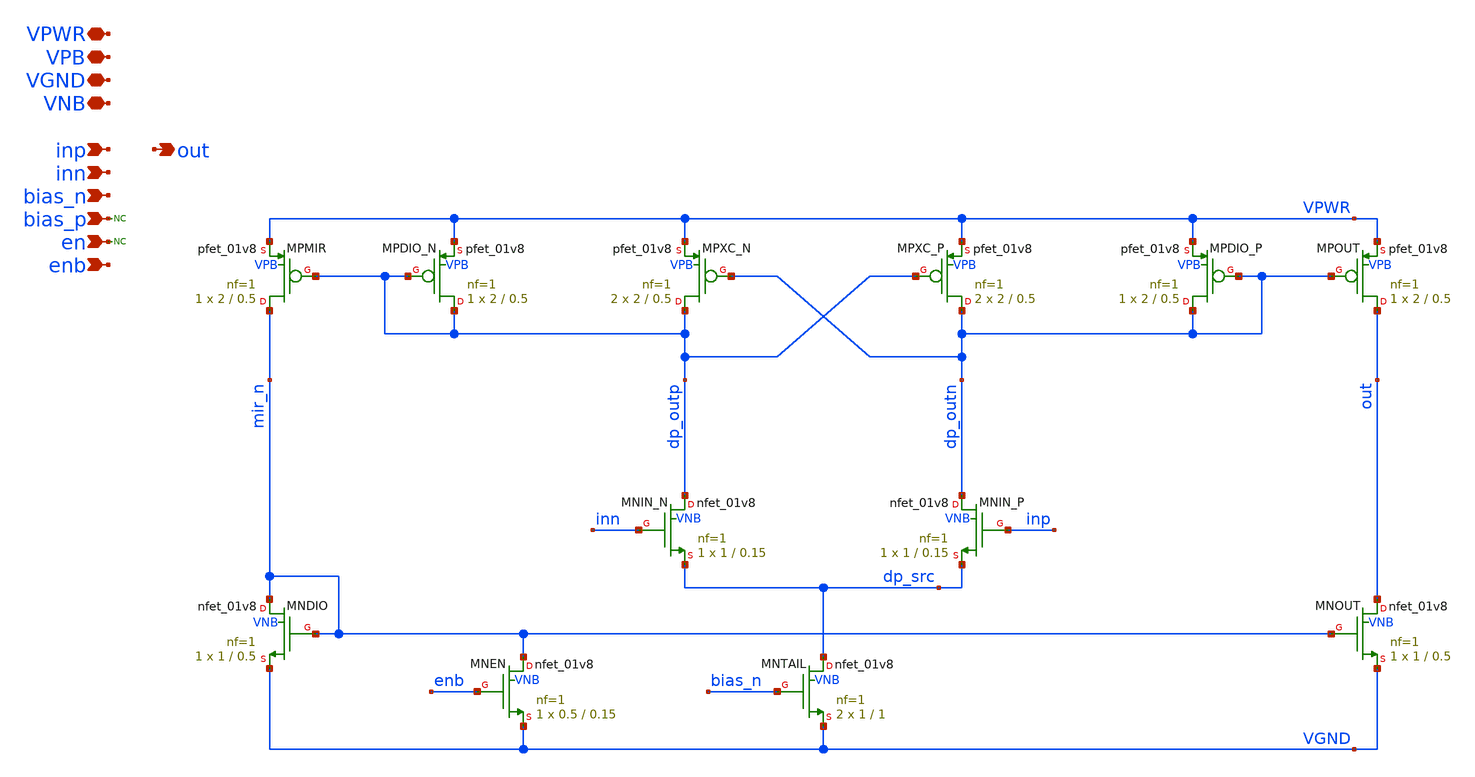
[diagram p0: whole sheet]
** sch_path: xschem/tiny_adc/tiny_adc_comp.sch
**.subckt tiny_adc_comp VPWR VPB VGND VNB inp out inn bias_n bias_p en enb
*.iopin VPWR
*.iopin VPB
*.iopin VGND
*.iopin VNB
*.ipin inp
*.opin out
*.ipin inn
*.ipin bias_n
*.ipin bias_p
*.ipin en
*.ipin enb
XMNIN_N dp_outp inn dp_src VNB sky130_fd_pr__nfet_01v8 L=0.15 W=1 nf=1 ad='int((nf+1)/2) * W/nf * 0.29'
+ as='int((nf+2)/2) * W/nf * 0.29' pd='2*int((nf+1)/2) * (W/nf + 0.29)' ps='2*int((nf+2)/2) * (W/nf + 0.29)'
+ nrd='0.29 / W' nrs='0.29 / W' sa=0 sb=0 sd=0 mult=1 m=1
XMNIN_P dp_outn inp dp_src VNB sky130_fd_pr__nfet_01v8 L=0.15 W=1 nf=1 ad='int((nf+1)/2) * W/nf * 0.29'
+ as='int((nf+2)/2) * W/nf * 0.29' pd='2*int((nf+1)/2) * (W/nf + 0.29)' ps='2*int((nf+2)/2) * (W/nf + 0.29)'
+ nrd='0.29 / W' nrs='0.29 / W' sa=0 sb=0 sd=0 mult=1 m=1
XMNTAIL dp_src bias_n VGND VNB sky130_fd_pr__nfet_01v8 L=1 W=1 nf=1 ad='int((nf+1)/2) * W/nf * 0.29'
+ as='int((nf+2)/2) * W/nf * 0.29' pd='2*int((nf+1)/2) * (W/nf + 0.29)' ps='2*int((nf+2)/2) * (W/nf + 0.29)'
+ nrd='0.29 / W' nrs='0.29 / W' sa=0 sb=0 sd=0 mult=2 m=2
XMPXC_P dp_outn dp_outp VPWR VPB sky130_fd_pr__pfet_01v8 L=0.5 W=2 nf=1 ad='int((nf+1)/2) * W/nf * 0.29'
+ as='int((nf+2)/2) * W/nf * 0.29' pd='2*int((nf+1)/2) * (W/nf + 0.29)' ps='2*int((nf+2)/2) * (W/nf + 0.29)'
+ nrd='0.29 / W' nrs='0.29 / W' sa=0 sb=0 sd=0 mult=2 m=2
XMPXC_N dp_outp dp_outn VPWR VPB sky130_fd_pr__pfet_01v8 L=0.5 W=2 nf=1 ad='int((nf+1)/2) * W/nf * 0.29'
+ as='int((nf+2)/2) * W/nf * 0.29' pd='2*int((nf+1)/2) * (W/nf + 0.29)' ps='2*int((nf+2)/2) * (W/nf + 0.29)'
+ nrd='0.29 / W' nrs='0.29 / W' sa=0 sb=0 sd=0 mult=2 m=2
XMPDIO_P dp_outn dp_outn VPWR VPB sky130_fd_pr__pfet_01v8 L=0.5 W=2 nf=1 ad='int((nf+1)/2) * W/nf * 0.29'
+ as='int((nf+2)/2) * W/nf * 0.29' pd='2*int((nf+1)/2) * (W/nf + 0.29)' ps='2*int((nf+2)/2) * (W/nf + 0.29)'
+ nrd='0.29 / W' nrs='0.29 / W' sa=0 sb=0 sd=0 mult=1 m=1
XMPDIO_N dp_outp dp_outp VPWR VPB sky130_fd_pr__pfet_01v8 L=0.5 W=2 nf=1 ad='int((nf+1)/2) * W/nf * 0.29'
+ as='int((nf+2)/2) * W/nf * 0.29' pd='2*int((nf+1)/2) * (W/nf + 0.29)' ps='2*int((nf+2)/2) * (W/nf + 0.29)'
+ nrd='0.29 / W' nrs='0.29 / W' sa=0 sb=0 sd=0 mult=1 m=1
XMNOUT out mir_n VGND VNB sky130_fd_pr__nfet_01v8 L=0.5 W=1 nf=1 ad='int((nf+1)/2) * W/nf * 0.29' as='int((nf+2)/2) * W/nf * 0.29'
+ pd='2*int((nf+1)/2) * (W/nf + 0.29)' ps='2*int((nf+2)/2) * (W/nf + 0.29)' nrd='0.29 / W' nrs='0.29 / W'
+ sa=0 sb=0 sd=0 mult=1 m=1
XMNDIO mir_n mir_n VGND VNB sky130_fd_pr__nfet_01v8 L=0.5 W=1 nf=1 ad='int((nf+1)/2) * W/nf * 0.29' as='int((nf+2)/2) * W/nf * 0.29'
+ pd='2*int((nf+1)/2) * (W/nf + 0.29)' ps='2*int((nf+2)/2) * (W/nf + 0.29)' nrd='0.29 / W' nrs='0.29 / W'
+ sa=0 sb=0 sd=0 mult=1 m=1
XMPOUT out dp_outn VPWR VPB sky130_fd_pr__pfet_01v8 L=0.5 W=2 nf=1 ad='int((nf+1)/2) * W/nf * 0.29' as='int((nf+2)/2) * W/nf * 0.29'
+ pd='2*int((nf+1)/2) * (W/nf + 0.29)' ps='2*int((nf+2)/2) * (W/nf + 0.29)' nrd='0.29 / W' nrs='0.29 / W'
+ sa=0 sb=0 sd=0 mult=1 m=1
XMPMIR mir_n dp_outp VPWR VPB sky130_fd_pr__pfet_01v8 L=0.5 W=2 nf=1 ad='int((nf+1)/2) * W/nf * 0.29'
+ as='int((nf+2)/2) * W/nf * 0.29' pd='2*int((nf+1)/2) * (W/nf + 0.29)' ps='2*int((nf+2)/2) * (W/nf + 0.29)'
+ nrd='0.29 / W' nrs='0.29 / W' sa=0 sb=0 sd=0 mult=1 m=1
* noconn bias_p
XMNEN mir_n enb VGND VNB sky130_fd_pr__nfet_01v8 L=0.15 W=0.5 nf=1 ad='int((nf+1)/2) * W/nf * 0.29' as='int((nf+2)/2) * W/nf * 0.29'
+ pd='2*int((nf+1)/2) * (W/nf + 0.29)' ps='2*int((nf+2)/2) * (W/nf + 0.29)' nrd='0.29 / W' nrs='0.29 / W'
+ sa=0 sb=0 sd=0 mult=1 m=1
* noconn en
**.ends
.end
